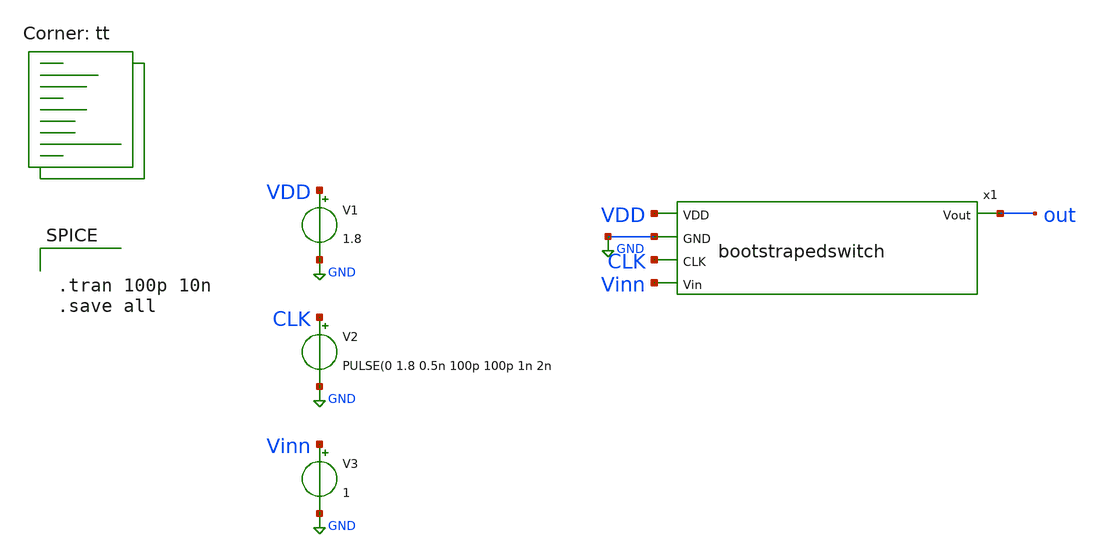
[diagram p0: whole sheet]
** sch_path: xschem/bstest.sch
**.subckt bstest
x1 VDD GND CLK Vinn out bootstrapedswitch
V2 CLK GND PULSE(0 1.8 0.5n 100p 100p 1n 2n
V1 VDD GND 1.8
V3 Vinn GND 1
**** begin user architecture code
.lib $::SKYWATER_MODELS/sky130.lib.spice tt


.tran 100p 10n
.save all


**** end user architecture code
**.ends
.GLOBAL GND
.end
